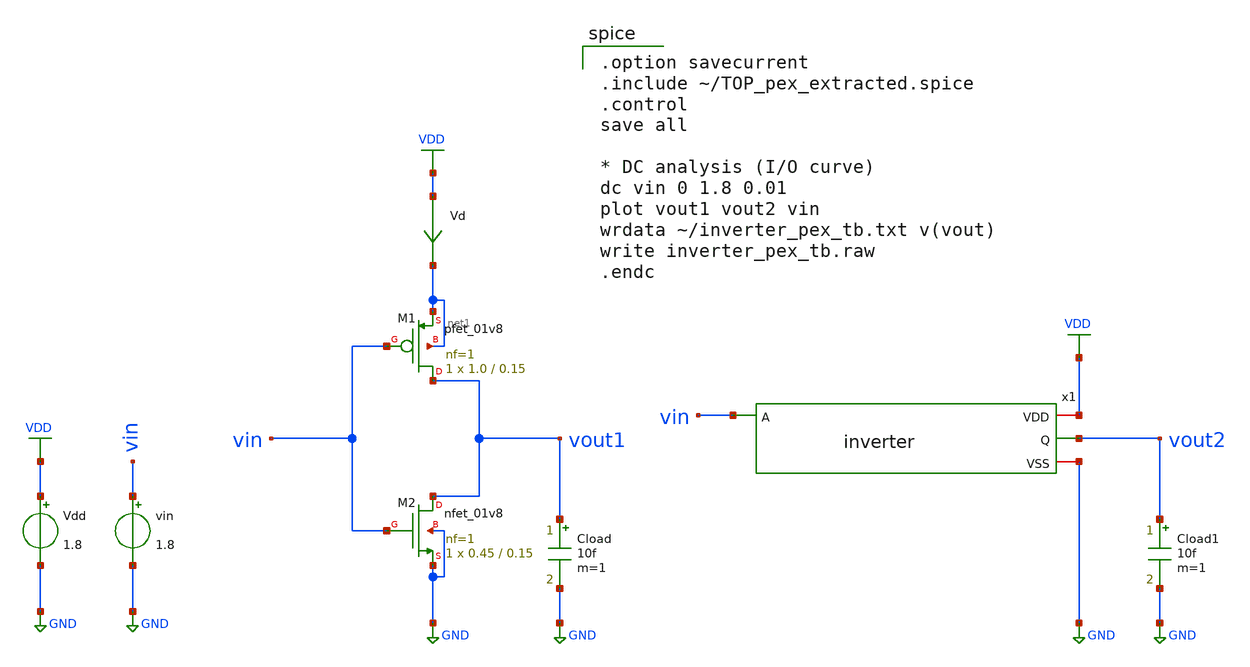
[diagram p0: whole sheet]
** sch_path: samples/inverter/SKY130/inverter_pex_tb.sch
**.subckt inverter_pex_tb
Vdd VDD GND 1.8
vin vin GND 1.8
Vd VDD net1 0
.save i(vd)
Cload vout1 GND 10f m=1
XM1 vout1 vin net1 net1 sky130_fd_pr__pfet_01v8 L=0.15 W=1.0 nf=1 ad='int((1 + 1)/2) * 1.0 / 1 * 0.29'
+ as='int((1 + 2)/2) * 1.0 / 1 * 0.29' pd='2*int((1 + 1)/2) * (1.0 / 1 + 0.29)' ps='2*int((1 + 2)/2) * (1.0 / 1 + 0.29)'
+ nrd='0.29 / 1.0 ' nrs='0.29 / 1.0 ' sa=0 sb=0 sd=0 mult=1 m=1
XM2 vout1 vin GND GND sky130_fd_pr__nfet_01v8 L=0.15 W=0.45 nf=1 ad='int((1 + 1)/2) * 0.45 / 1 * 0.29'
+ as='int((1 + 2)/2) * 0.45 / 1 * 0.29' pd='2*int((1 + 1)/2) * (0.45 / 1 + 0.29)' ps='2*int((1 + 2)/2) * (0.45 / 1 + 0.29)'
+ nrd='0.29 / 0.45 ' nrs='0.29 / 0.45 ' sa=0 sb=0 sd=0 mult=1 m=1
x1 VDD vin vout2 GND TOP
Cload1 vout2 GND 10f m=1
**** begin user architecture code

.option savecurrent
.include ~/TOP_pex_extracted.spice
.control
save all

* DC analysis (I/O curve)
dc vin 0 1.8 0.01
plot vout1 vout2 vin
wrdata ~/inverter_pex_tb.txt v(vout)
write inverter_pex_tb.raw
.endc


** opencircuitdesign pdks install
.lib $::SKYWATER_MODELS/sky130.lib.spice tt

**** end user architecture code
**.ends
.GLOBAL GND
.GLOBAL VDD
.end
